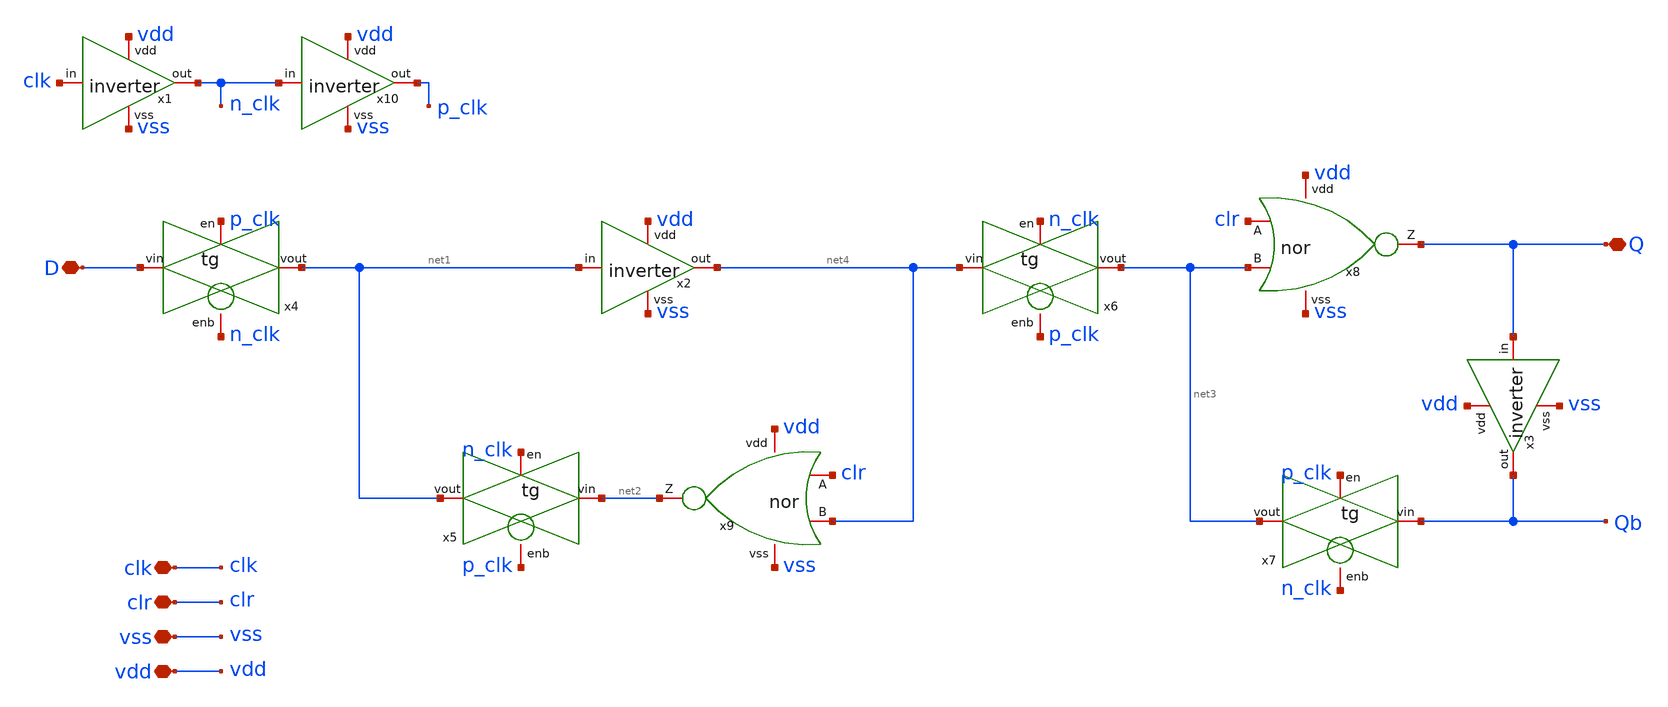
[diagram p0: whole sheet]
** sch_path: designs/dffc.sch
**.subckt dffc clk clr vss vdd D Q
*.iopin clk
*.iopin clr
*.iopin vss
*.iopin vdd
*.iopin D
*.iopin Q
x1 vdd n_clk clk vss inverter
x2 vdd net4 net1 vss inverter
x3 vdd Qb Q vss inverter
x4 D n_clk p_clk net1 tg
x8 vdd Q clr net3 vss nor
x9 vdd net2 clr net4 vss nor
x5 net2 p_clk n_clk net1 tg
x6 net4 p_clk n_clk net3 tg
x7 Qb n_clk p_clk net3 tg
x10 vdd p_clk n_clk vss inverter
**.ends

* expanding   symbol:  /foss/designs/inverter.sym # of pins=4
** sym_path: designs/inverter.sym
** sch_path: designs/inverter.sch
.subckt inverter vdd out in vss
*.iopin out
*.iopin vss
*.iopin vdd
*.iopin in
XM2 out in vss vss sky130_fd_pr__nfet_01v8 L=0.15 W=0.75 nf=1 ad='int((nf+1)/2) * W/nf * 0.29' as='int((nf+2)/2) * W/nf * 0.29'
+ pd='2*int((nf+1)/2) * (W/nf + 0.29)' ps='2*int((nf+2)/2) * (W/nf + 0.29)' nrd='0.29 / W' nrs='0.29 / W'
+ sa=0 sb=0 sd=0 mult=1 m=1
XM1 out in vdd vdd sky130_fd_pr__pfet_01v8 L=0.15 W=1.5 nf=1 ad='int((nf+1)/2) * W/nf * 0.29' as='int((nf+2)/2) * W/nf * 0.29'
+ pd='2*int((nf+1)/2) * (W/nf + 0.29)' ps='2*int((nf+2)/2) * (W/nf + 0.29)' nrd='0.29 / W' nrs='0.29 / W'
+ sa=0 sb=0 sd=0 mult=1 m=1
.ends


* expanding   symbol:  /foss/designs/tg.sym # of pins=4
** sym_path: designs/tg.sym
** sch_path: designs/tg.sch
.subckt tg vin enb en vout
*.iopin vin
*.iopin vout
*.iopin enb
*.iopin en
XM1 vin en vout enb sky130_fd_pr__nfet_01v8 L=0.15 W=0.75 nf=1 ad='int((nf+1)/2) * W/nf * 0.29' as='int((nf+2)/2) * W/nf * 0.29'
+ pd='2*int((nf+1)/2) * (W/nf + 0.29)' ps='2*int((nf+2)/2) * (W/nf + 0.29)' nrd='0.29 / W' nrs='0.29 / W'
+ sa=0 sb=0 sd=0 mult=1 m=1
XM2 vout enb vin en sky130_fd_pr__pfet_01v8 L=0.15 W=1.5 nf=1 ad='int((nf+1)/2) * W/nf * 0.29' as='int((nf+2)/2) * W/nf * 0.29'
+ pd='2*int((nf+1)/2) * (W/nf + 0.29)' ps='2*int((nf+2)/2) * (W/nf + 0.29)' nrd='0.29 / W' nrs='0.29 / W'
+ sa=0 sb=0 sd=0 mult=1 m=1
.ends


* expanding   symbol:  /foss/designs/nor.sym # of pins=5
** sym_path: designs/sch/nor.sym
** sch_path: designs/sch/nor.sch
.subckt nor vdd Z A B vss
*.iopin A
*.iopin B
*.iopin vdd
*.iopin Z
*.iopin vss
XM1 Z A vss vss sky130_fd_pr__nfet_01v8 L=0.15 W=0.75 nf=1 ad='int((nf+1)/2) * W/nf * 0.29' as='int((nf+2)/2) * W/nf * 0.29'
+ pd='2*int((nf+1)/2) * (W/nf + 0.29)' ps='2*int((nf+2)/2) * (W/nf + 0.29)' nrd='0.29 / W' nrs='0.29 / W'
+ sa=0 sb=0 sd=0 mult=1 m=1
XM4 net1 B vdd vdd sky130_fd_pr__pfet_01v8 L=0.15 W=3 nf=1 ad='int((nf+1)/2) * W/nf * 0.29' as='int((nf+2)/2) * W/nf * 0.29'
+ pd='2*int((nf+1)/2) * (W/nf + 0.29)' ps='2*int((nf+2)/2) * (W/nf + 0.29)' nrd='0.29 / W' nrs='0.29 / W'
+ sa=0 sb=0 sd=0 mult=1 m=1
XM2 Z B vss vss sky130_fd_pr__nfet_01v8 L=0.15 W=0.75 nf=1 ad='int((nf+1)/2) * W/nf * 0.29' as='int((nf+2)/2) * W/nf * 0.29'
+ pd='2*int((nf+1)/2) * (W/nf + 0.29)' ps='2*int((nf+2)/2) * (W/nf + 0.29)' nrd='0.29 / W' nrs='0.29 / W'
+ sa=0 sb=0 sd=0 mult=1 m=1
XM3 Z A net1 vdd sky130_fd_pr__pfet_01v8 L=0.15 W=3 nf=1 ad='int((nf+1)/2) * W/nf * 0.29' as='int((nf+2)/2) * W/nf * 0.29'
+ pd='2*int((nf+1)/2) * (W/nf + 0.29)' ps='2*int((nf+2)/2) * (W/nf + 0.29)' nrd='0.29 / W' nrs='0.29 / W'
+ sa=0 sb=0 sd=0 mult=1 m=1
.ends

.end
